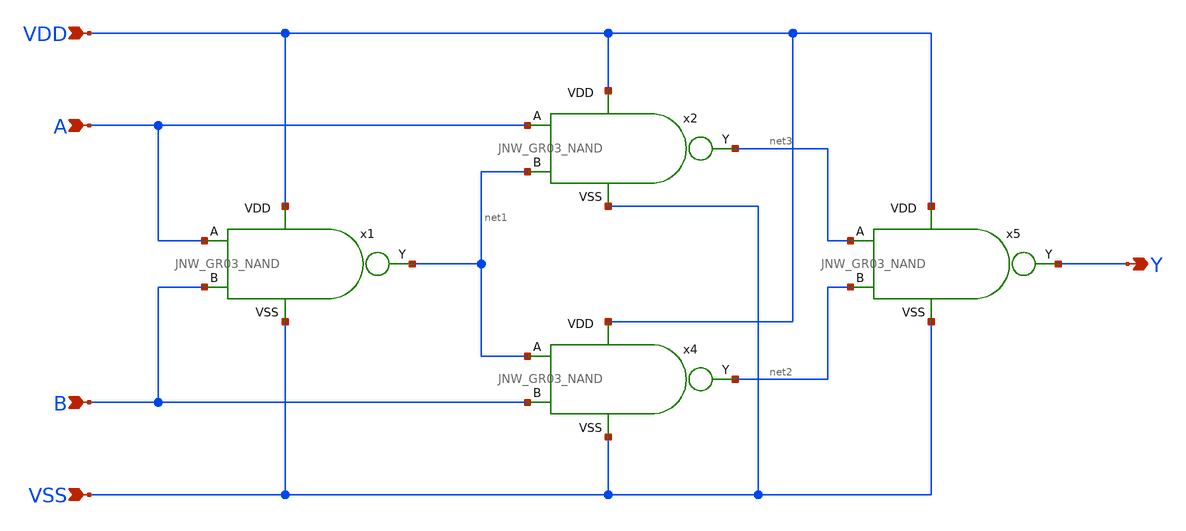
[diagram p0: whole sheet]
** sch_path: design/JNW_GR03_SKY130A/JNW_GR03_XOR.sch
**.subckt JNW_GR03_XOR VDD Y VSS A B
*.ipin VDD
*.opin Y
*.ipin VSS
*.ipin A
*.ipin B
x2 VDD net3 A net1 VSS JNW_GR03_NAND
x4 VDD net2 net1 B VSS JNW_GR03_NAND
x5 VDD Y net3 net2 VSS JNW_GR03_NAND
x1 VDD net1 A B VSS JNW_GR03_NAND
**.ends
.end
